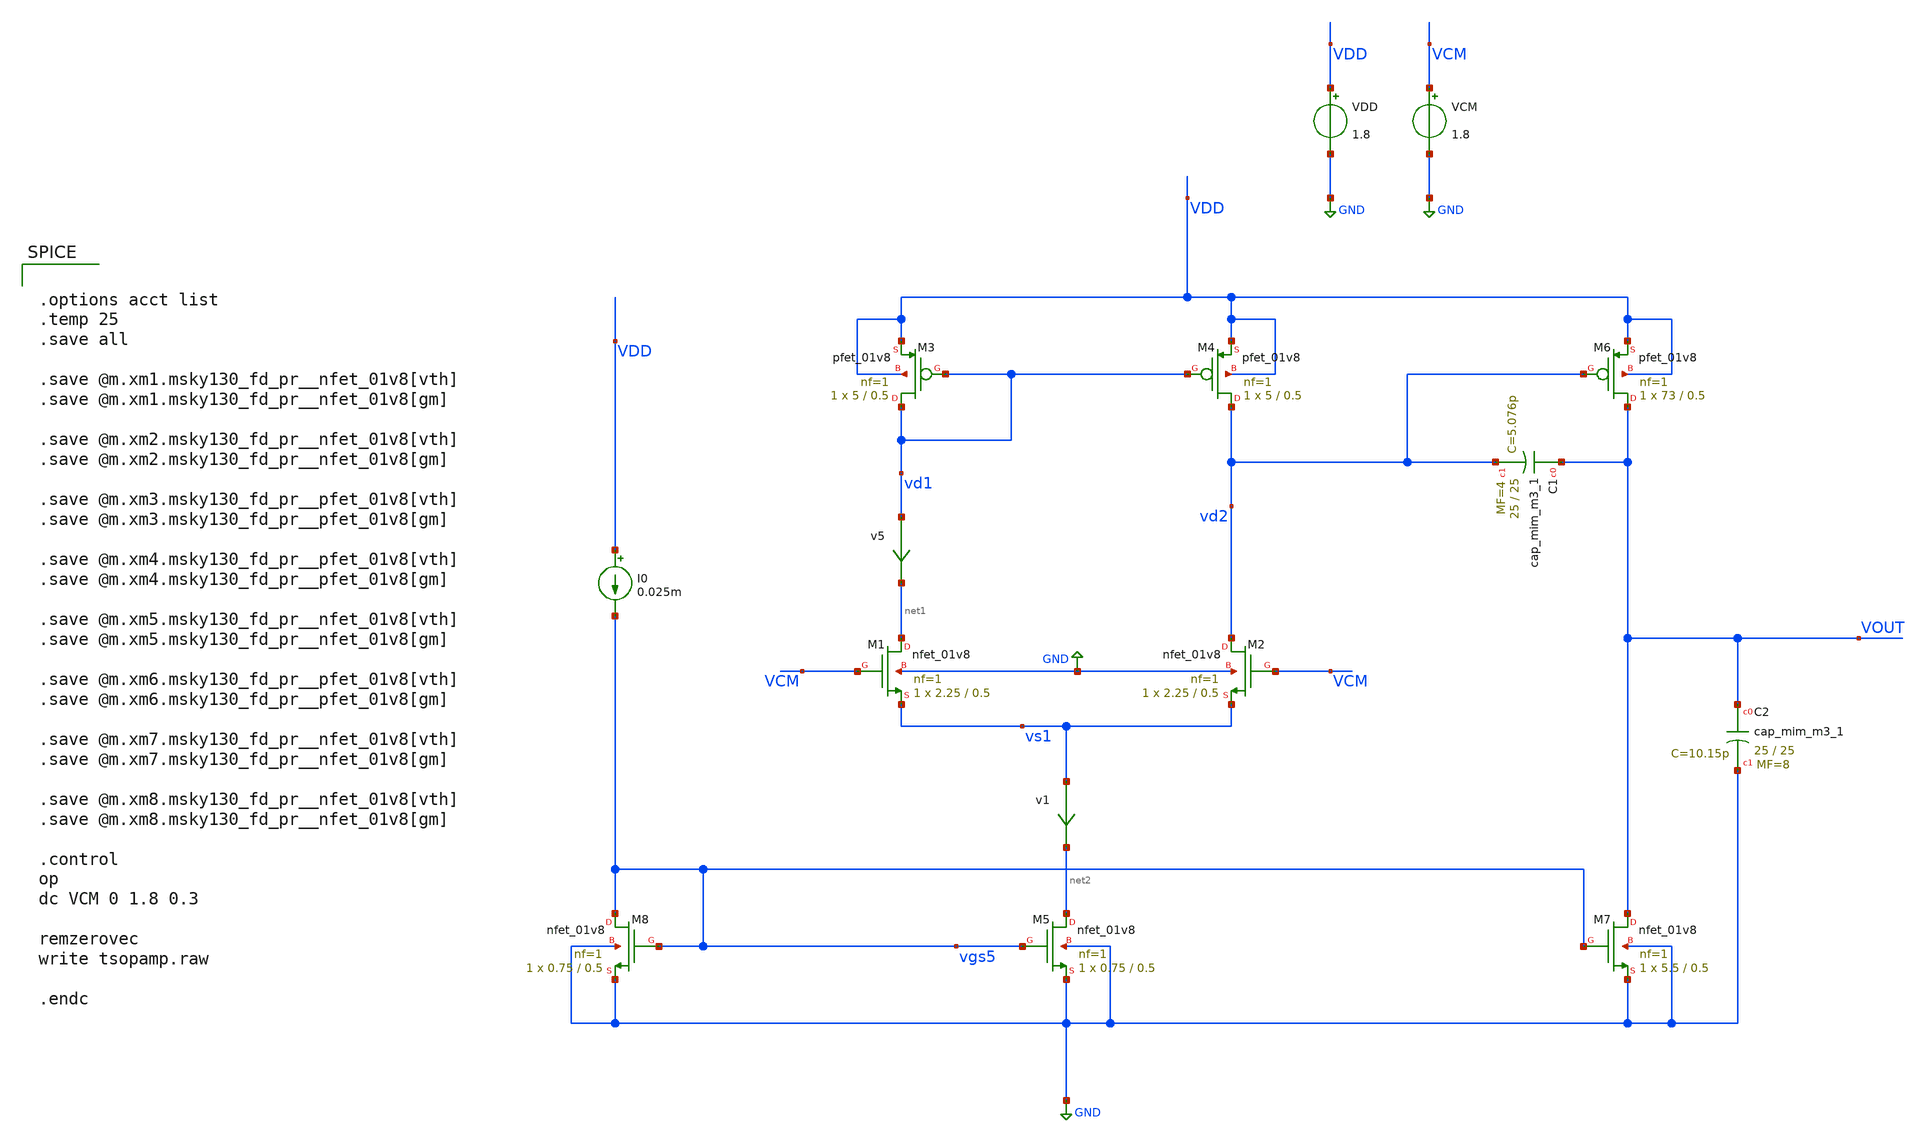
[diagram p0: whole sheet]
** sch_path: xschem/tsopamp.sch
**.subckt tsopamp
XM1 net1 VCM vs1 GND sky130_fd_pr__nfet_01v8 L=0.5 W=2.25 nf=1 ad='int((nf+1)/2) * W/nf * 0.29' as='int((nf+2)/2) * W/nf * 0.29'
+ pd='2*int((nf+1)/2) * (W/nf + 0.29)' ps='2*int((nf+2)/2) * (W/nf + 0.29)' nrd='0.29 / W' nrs='0.29 / W'
+ sa=0 sb=0 sd=0 mult=1 m=1
XM2 vd2 VCM vs1 GND sky130_fd_pr__nfet_01v8 L=0.5 W=2.25 nf=1 ad='int((nf+1)/2) * W/nf * 0.29' as='int((nf+2)/2) * W/nf * 0.29'
+ pd='2*int((nf+1)/2) * (W/nf + 0.29)' ps='2*int((nf+2)/2) * (W/nf + 0.29)' nrd='0.29 / W' nrs='0.29 / W'
+ sa=0 sb=0 sd=0 mult=1 m=1
XM3 vd1 vd1 VDD VDD sky130_fd_pr__pfet_01v8 L=0.5 W=5 nf=1 ad='int((nf+1)/2) * W/nf * 0.29' as='int((nf+2)/2) * W/nf * 0.29'
+ pd='2*int((nf+1)/2) * (W/nf + 0.29)' ps='2*int((nf+2)/2) * (W/nf + 0.29)' nrd='0.29 / W' nrs='0.29 / W'
+ sa=0 sb=0 sd=0 mult=1 m=1
XM4 vd2 vd1 VDD VDD sky130_fd_pr__pfet_01v8 L=0.5 W=5 nf=1 ad='int((nf+1)/2) * W/nf * 0.29' as='int((nf+2)/2) * W/nf * 0.29'
+ pd='2*int((nf+1)/2) * (W/nf + 0.29)' ps='2*int((nf+2)/2) * (W/nf + 0.29)' nrd='0.29 / W' nrs='0.29 / W'
+ sa=0 sb=0 sd=0 mult=1 m=1
XM5 net2 vgs5 GND GND sky130_fd_pr__nfet_01v8 L=0.5 W=0.75 nf=1 ad='int((nf+1)/2) * W/nf * 0.29' as='int((nf+2)/2) * W/nf * 0.29'
+ pd='2*int((nf+1)/2) * (W/nf + 0.29)' ps='2*int((nf+2)/2) * (W/nf + 0.29)' nrd='0.29 / W' nrs='0.29 / W'
+ sa=0 sb=0 sd=0 mult=1 m=1
XM6 VOUT vd2 VDD VDD sky130_fd_pr__pfet_01v8 L=0.5 W=73 nf=1 ad='int((nf+1)/2) * W/nf * 0.29' as='int((nf+2)/2) * W/nf * 0.29'
+ pd='2*int((nf+1)/2) * (W/nf + 0.29)' ps='2*int((nf+2)/2) * (W/nf + 0.29)' nrd='0.29 / W' nrs='0.29 / W'
+ sa=0 sb=0 sd=0 mult=1 m=1
XM7 VOUT vgs5 GND GND sky130_fd_pr__nfet_01v8 L=0.5 W=5.5 nf=1 ad='int((nf+1)/2) * W/nf * 0.29' as='int((nf+2)/2) * W/nf * 0.29'
+ pd='2*int((nf+1)/2) * (W/nf + 0.29)' ps='2*int((nf+2)/2) * (W/nf + 0.29)' nrd='0.29 / W' nrs='0.29 / W'
+ sa=0 sb=0 sd=0 mult=1 m=1
XM8 vgs5 vgs5 GND GND sky130_fd_pr__nfet_01v8 L=0.5 W=0.75 nf=1 ad='int((nf+1)/2) * W/nf * 0.29' as='int((nf+2)/2) * W/nf * 0.29'
+ pd='2*int((nf+1)/2) * (W/nf + 0.29)' ps='2*int((nf+2)/2) * (W/nf + 0.29)' nrd='0.29 / W' nrs='0.29 / W'
+ sa=0 sb=0 sd=0 mult=1 m=1
XC1 VOUT vd2 sky130_fd_pr__cap_mim_m3_1 W=25 L=25 MF=4 m=4
XC2 VOUT GND sky130_fd_pr__cap_mim_m3_1 W=25 L=25 MF=8 m=8
I0 VDD vgs5 0.025m
VDD VDD GND 1.8
VCM VCM GND 1.8
v5 vd1 net1 0
.save i(v5)
v1 vs1 net2 0
.save i(v1)
**** begin user architecture code


.options acct list
.temp 25
.save all

.save @m.xm1.msky130_fd_pr__nfet_01v8[vth]
.save @m.xm1.msky130_fd_pr__nfet_01v8[gm]

.save @m.xm2.msky130_fd_pr__nfet_01v8[vth]
.save @m.xm2.msky130_fd_pr__nfet_01v8[gm]

.save @m.xm3.msky130_fd_pr__pfet_01v8[vth]
.save @m.xm3.msky130_fd_pr__pfet_01v8[gm]

.save @m.xm4.msky130_fd_pr__pfet_01v8[vth]
.save @m.xm4.msky130_fd_pr__pfet_01v8[gm]

.save @m.xm5.msky130_fd_pr__nfet_01v8[vth]
.save @m.xm5.msky130_fd_pr__nfet_01v8[gm]

.save @m.xm6.msky130_fd_pr__pfet_01v8[vth]
.save @m.xm6.msky130_fd_pr__pfet_01v8[gm]

.save @m.xm7.msky130_fd_pr__nfet_01v8[vth]
.save @m.xm7.msky130_fd_pr__nfet_01v8[gm]

.save @m.xm8.msky130_fd_pr__nfet_01v8[vth]
.save @m.xm8.msky130_fd_pr__nfet_01v8[gm]

.control
op
dc VCM 0 1.8 0.3

remzerovec
write tsopamp.raw

.endc




** opencircuitdesign pdks install
.lib $::SKYWATER_MODELS/sky130.lib.spice tt


**** end user architecture code
**.ends
.GLOBAL GND
.end
